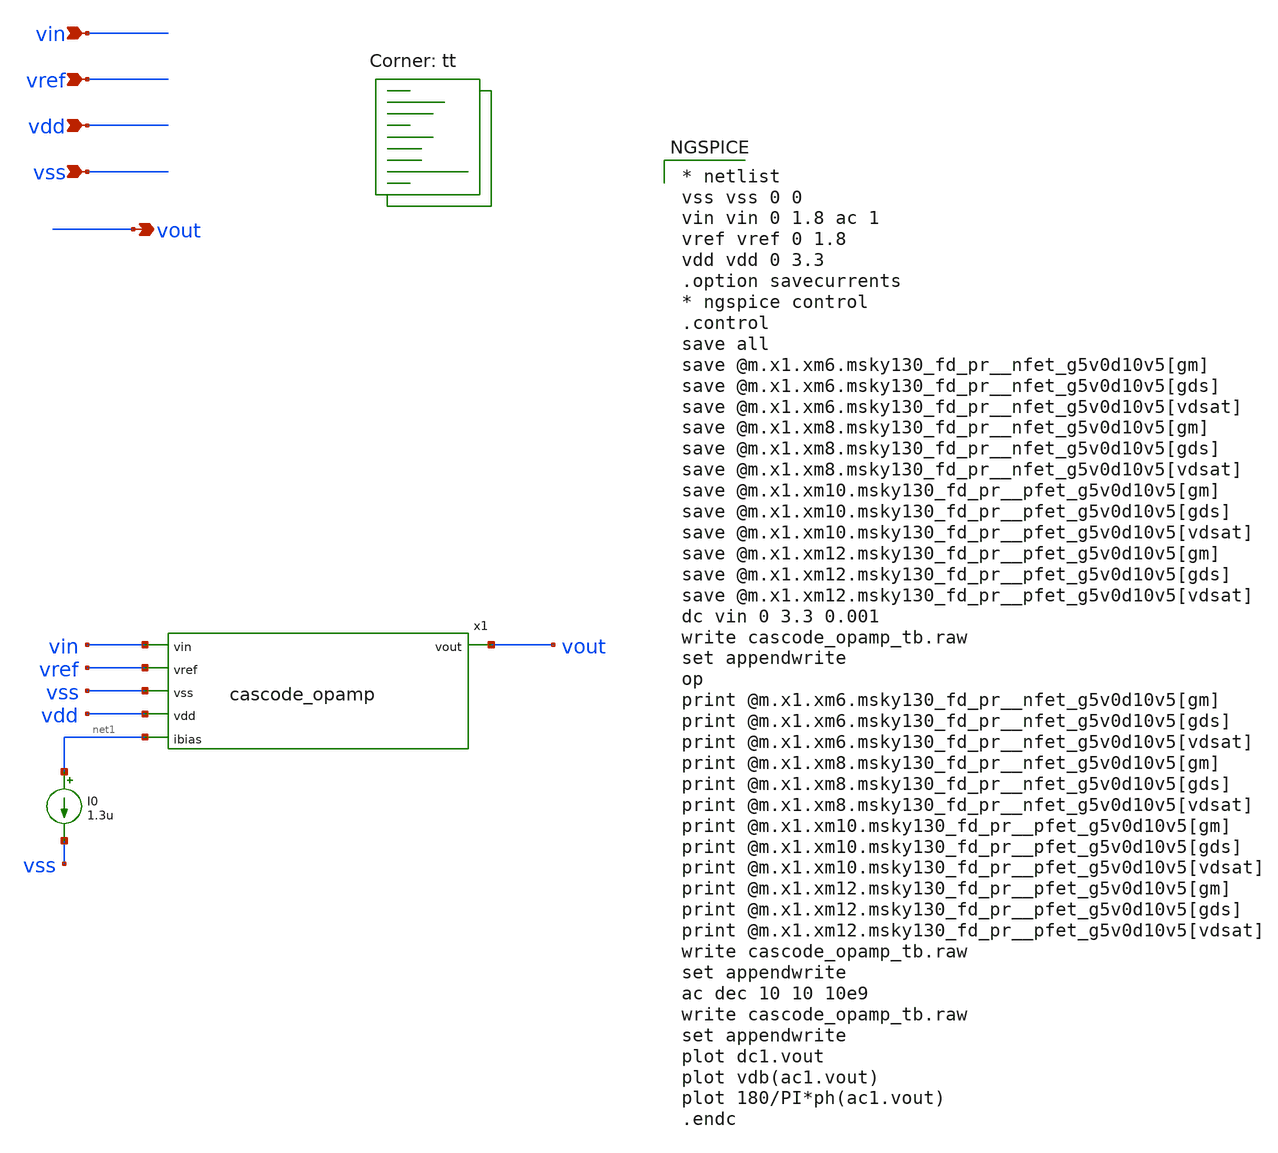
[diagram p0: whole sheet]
** sch_path: xschem/cascode_opamp_tb.sch
**.subckt cascode_opamp_tb vss vout vdd vref vin
*.ipin vss
*.opin vout
*.ipin vdd
*.ipin vref
*.ipin vin
x1 vout vin vref vss vdd net1 cascode_opamp
I0 net1 vss 1.3u
**** begin user architecture code

* netlist
vss vss 0 0
vin vin 0 1.8 ac 1
vref vref 0 1.8
vdd vdd 0 3.3
.option savecurrents
* ngspice control
.control
save all
save @m.x1.xm6.msky130_fd_pr__nfet_g5v0d10v5[gm]
save @m.x1.xm6.msky130_fd_pr__nfet_g5v0d10v5[gds]
save @m.x1.xm6.msky130_fd_pr__nfet_g5v0d10v5[vdsat]
save @m.x1.xm8.msky130_fd_pr__nfet_g5v0d10v5[gm]
save @m.x1.xm8.msky130_fd_pr__nfet_g5v0d10v5[gds]
save @m.x1.xm8.msky130_fd_pr__nfet_g5v0d10v5[vdsat]
save @m.x1.xm10.msky130_fd_pr__pfet_g5v0d10v5[gm]
save @m.x1.xm10.msky130_fd_pr__pfet_g5v0d10v5[gds]
save @m.x1.xm10.msky130_fd_pr__pfet_g5v0d10v5[vdsat]
save @m.x1.xm12.msky130_fd_pr__pfet_g5v0d10v5[gm]
save @m.x1.xm12.msky130_fd_pr__pfet_g5v0d10v5[gds]
save @m.x1.xm12.msky130_fd_pr__pfet_g5v0d10v5[vdsat]
dc vin 0 3.3 0.001
write cascode_opamp_tb.raw
set appendwrite
op
print @m.x1.xm6.msky130_fd_pr__nfet_g5v0d10v5[gm]
print @m.x1.xm6.msky130_fd_pr__nfet_g5v0d10v5[gds]
print @m.x1.xm6.msky130_fd_pr__nfet_g5v0d10v5[vdsat]
print @m.x1.xm8.msky130_fd_pr__nfet_g5v0d10v5[gm]
print @m.x1.xm8.msky130_fd_pr__nfet_g5v0d10v5[gds]
print @m.x1.xm8.msky130_fd_pr__nfet_g5v0d10v5[vdsat]
print @m.x1.xm10.msky130_fd_pr__pfet_g5v0d10v5[gm]
print @m.x1.xm10.msky130_fd_pr__pfet_g5v0d10v5[gds]
print @m.x1.xm10.msky130_fd_pr__pfet_g5v0d10v5[vdsat]
print @m.x1.xm12.msky130_fd_pr__pfet_g5v0d10v5[gm]
print @m.x1.xm12.msky130_fd_pr__pfet_g5v0d10v5[gds]
print @m.x1.xm12.msky130_fd_pr__pfet_g5v0d10v5[vdsat]
write cascode_opamp_tb.raw
set appendwrite
ac dec 10 10 10e9
write cascode_opamp_tb.raw
set appendwrite
plot dc1.vout
plot vdb(ac1.vout)
plot 180/PI*ph(ac1.vout)
.endc


.lib $::SKYWATER_MODELS/sky130.lib.spice tt
**** end user architecture code
**.ends

* expanding   symbol:  cascode_opamp.sym # of pins=6
** sym_path: xschem/cascode_opamp.sym
** sch_path: xschem/cascode_opamp.sch
.subckt cascode_opamp vout vin vref vss vdd ibias
*.ipin vin
*.ipin vref
*.ipin vss
*.opin vout
*.ipin vdd
*.ipin ibias
XM5 net1 vin ibias vss sky130_fd_pr__nfet_g5v0d10v5 L=1 W=1 nf=1 ad='int((nf+1)/2) * W/nf * 0.29' as='int((nf+2)/2) * W/nf * 0.29'
+ pd='2*int((nf+1)/2) * (W/nf + 0.29)' ps='2*int((nf+2)/2) * (W/nf + 0.29)' nrd='0.29 / W' nrs='0.29 / W'
+ sa=0 sb=0 sd=0 mult=1 m=1
XM6 vx vref ibias vss sky130_fd_pr__nfet_g5v0d10v5 L=1 W=1 nf=1 ad='int((nf+1)/2) * W/nf * 0.29' as='int((nf+2)/2) * W/nf * 0.29'
+ pd='2*int((nf+1)/2) * (W/nf + 0.29)' ps='2*int((nf+2)/2) * (W/nf + 0.29)' nrd='0.29 / W' nrs='0.29 / W'
+ sa=0 sb=0 sd=0 mult=1 m=1
XM7 vb3 vb1 net1 vss sky130_fd_pr__nfet_g5v0d10v5 L=1 W=1 nf=1 ad='int((nf+1)/2) * W/nf * 0.29' as='int((nf+2)/2) * W/nf * 0.29'
+ pd='2*int((nf+1)/2) * (W/nf + 0.29)' ps='2*int((nf+2)/2) * (W/nf + 0.29)' nrd='0.29 / W' nrs='0.29 / W'
+ sa=0 sb=0 sd=0 mult=1 m=1
XM8 vout vb1 vx vss sky130_fd_pr__nfet_g5v0d10v5 L=1 W=1 nf=1 ad='int((nf+1)/2) * W/nf * 0.29' as='int((nf+2)/2) * W/nf * 0.29'
+ pd='2*int((nf+1)/2) * (W/nf + 0.29)' ps='2*int((nf+2)/2) * (W/nf + 0.29)' nrd='0.29 / W' nrs='0.29 / W'
+ sa=0 sb=0 sd=0 mult=1 m=1
XM9 vb3 vb2 net2 vdd sky130_fd_pr__pfet_g5v0d10v5 L=5 W=1 nf=1 ad='int((nf+1)/2) * W/nf * 0.29' as='int((nf+2)/2) * W/nf * 0.29'
+ pd='2*int((nf+1)/2) * (W/nf + 0.29)' ps='2*int((nf+2)/2) * (W/nf + 0.29)' nrd='0.29 / W' nrs='0.29 / W'
+ sa=0 sb=0 sd=0 mult=1 m=1
XM10 vout vb2 vy vdd sky130_fd_pr__pfet_g5v0d10v5 L=5 W=1 nf=1 ad='int((nf+1)/2) * W/nf * 0.29' as='int((nf+2)/2) * W/nf * 0.29'
+ pd='2*int((nf+1)/2) * (W/nf + 0.29)' ps='2*int((nf+2)/2) * (W/nf + 0.29)' nrd='0.29 / W' nrs='0.29 / W'
+ sa=0 sb=0 sd=0 mult=1 m=1
XM11 net2 vb3 vdd vdd sky130_fd_pr__pfet_g5v0d10v5 L=5 W=1 nf=1 ad='int((nf+1)/2) * W/nf * 0.29' as='int((nf+2)/2) * W/nf * 0.29'
+ pd='2*int((nf+1)/2) * (W/nf + 0.29)' ps='2*int((nf+2)/2) * (W/nf + 0.29)' nrd='0.29 / W' nrs='0.29 / W'
+ sa=0 sb=0 sd=0 mult=1 m=1
XM12 vy vb3 vdd vdd sky130_fd_pr__pfet_g5v0d10v5 L=5 W=1 nf=1 ad='int((nf+1)/2) * W/nf * 0.29' as='int((nf+2)/2) * W/nf * 0.29'
+ pd='2*int((nf+1)/2) * (W/nf + 0.29)' ps='2*int((nf+2)/2) * (W/nf + 0.29)' nrd='0.29 / W' nrs='0.29 / W'
+ sa=0 sb=0 sd=0 mult=1 m=1
V1 vb1 vss 2.4
V2 vb2 vss 1
.ends

.end
